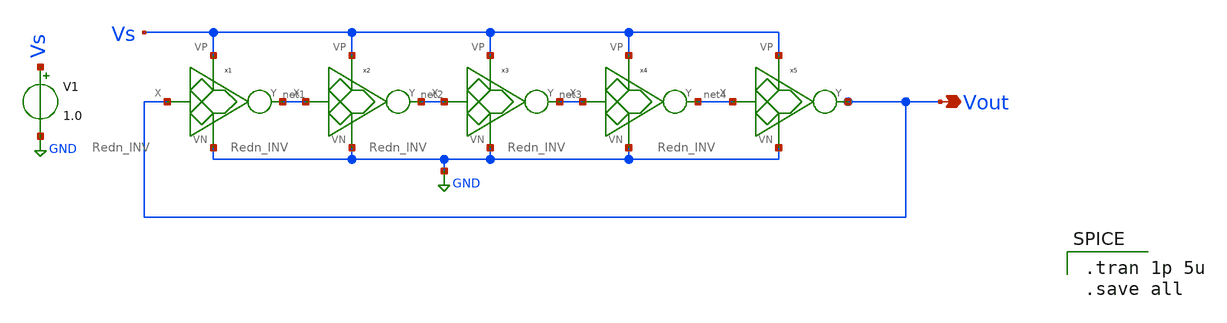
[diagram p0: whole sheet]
** sch_path: Blocks/Ring_Osci/Rdn_Rng_Osc.sch
**.subckt Rdn_Rng_Osc Vout
*.opin Vout
V1 Vs GND 1.0
x1 Vout net1 Vs GND Redn_INV
x2 net1 net2 Vs GND Redn_INV
x3 net2 net3 Vs GND Redn_INV
x4 net3 net4 Vs GND Redn_INV
x5 net4 Vout Vs GND Redn_INV
**** begin user architecture code

** opencircuitdesign pdks install
.lib $::SKYWATER_MODELS/sky130.lib.spice tt



.tran 1p 5u
.save all

**** end user architecture code
**.ends

* expanding   symbol:  Pico_project/Rdn_INV/Redn_INV.sym # of pins=4
** sym_path: component/Reduntant_Inverter/Redn_INV.sym
** sch_path: component/Reduntant_Inverter/Redn_INV.sch
.subckt Redn_INV X Y VP VN
*.opin Y
*.ipin X
*.iopin VP
*.iopin VN
XM15 net4 X VN VN sky130_fd_pr__nfet_01v8_lvt L=0.15 W=1 nf=1 ad='int((nf+1)/2) * W/nf * 0.29' as='int((nf+2)/2) * W/nf * 0.29'
+ pd='2*int((nf+1)/2) * (W/nf + 0.29)' ps='2*int((nf+2)/2) * (W/nf + 0.29)' nrd='0.29 / W' nrs='0.29 / W'
+ sa=0 sb=0 sd=0 mult=1 m=1
XM1 net5 X net3 VN sky130_fd_pr__nfet_01v8_lvt L=0.15 W=3.25 nf=1 ad='int((nf+1)/2) * W/nf * 0.29' as='int((nf+2)/2) * W/nf * 0.29'
+ pd='2*int((nf+1)/2) * (W/nf + 0.29)' ps='2*int((nf+2)/2) * (W/nf + 0.29)' nrd='0.29 / W' nrs='0.29 / W'
+ sa=0 sb=0 sd=0 mult=1 m=1
XM16 Y X net6 VN sky130_fd_pr__nfet_01v8_lvt L=0.15 W=6.5 nf=1 ad='int((nf+1)/2) * W/nf * 0.29' as='int((nf+2)/2) * W/nf * 0.29'
+ pd='2*int((nf+1)/2) * (W/nf + 0.29)' ps='2*int((nf+2)/2) * (W/nf + 0.29)' nrd='0.29 / W' nrs='0.29 / W'
+ sa=0 sb=0 sd=0 mult=1 m=1
XM17 net3 X VN VN sky130_fd_pr__nfet_01v8_lvt L=0.15 W=3.25 nf=1 ad='int((nf+1)/2) * W/nf * 0.29' as='int((nf+2)/2) * W/nf * 0.29'
+ pd='2*int((nf+1)/2) * (W/nf + 0.29)' ps='2*int((nf+2)/2) * (W/nf + 0.29)' nrd='0.29 / W' nrs='0.29 / W'
+ sa=0 sb=0 sd=0 mult=1 m=1
XM18 net2 X VN VN sky130_fd_pr__nfet_01v8_lvt L=0.15 W=1.5 nf=1 ad='int((nf+1)/2) * W/nf * 0.29' as='int((nf+2)/2) * W/nf * 0.29'
+ pd='2*int((nf+1)/2) * (W/nf + 0.29)' ps='2*int((nf+2)/2) * (W/nf + 0.29)' nrd='0.29 / W' nrs='0.29 / W'
+ sa=0 sb=0 sd=0 mult=1 m=1
XM19 net1 X VN VN sky130_fd_pr__nfet_01v8_lvt L=0.15 W=6.5 nf=1 ad='int((nf+1)/2) * W/nf * 0.29' as='int((nf+2)/2) * W/nf * 0.29'
+ pd='2*int((nf+1)/2) * (W/nf + 0.29)' ps='2*int((nf+2)/2) * (W/nf + 0.29)' nrd='0.29 / W' nrs='0.29 / W'
+ sa=0 sb=0 sd=0 mult=1 m=1
XM20 net6 X net1 VN sky130_fd_pr__nfet_01v8_lvt L=0.15 W=6.5 nf=1 ad='int((nf+1)/2) * W/nf * 0.29' as='int((nf+2)/2) * W/nf * 0.29'
+ pd='2*int((nf+1)/2) * (W/nf + 0.29)' ps='2*int((nf+2)/2) * (W/nf + 0.29)' nrd='0.29 / W' nrs='0.29 / W'
+ sa=0 sb=0 sd=0 mult=1 m=1
XM2 net4 X VP VP sky130_fd_pr__pfet_01v8 L=0.15 W=10 nf=1 ad='int((nf+1)/2) * W/nf * 0.29' as='int((nf+2)/2) * W/nf * 0.29'
+ pd='2*int((nf+1)/2) * (W/nf + 0.29)' ps='2*int((nf+2)/2) * (W/nf + 0.29)' nrd='0.29 / W' nrs='0.29 / W'
+ sa=0 sb=0 sd=0 mult=1 m=1
XM5 net5 X net4 net4 sky130_fd_pr__pfet_01v8 L=0.15 W=10 nf=1 ad='int((nf+1)/2) * W/nf * 0.29' as='int((nf+2)/2) * W/nf * 0.29'
+ pd='2*int((nf+1)/2) * (W/nf + 0.29)' ps='2*int((nf+2)/2) * (W/nf + 0.29)' nrd='0.29 / W' nrs='0.29 / W'
+ sa=0 sb=0 sd=0 mult=1 m=1
XM6 Y X net5 VP sky130_fd_pr__pfet_01v8 L=0.15 W=10 nf=1 ad='int((nf+1)/2) * W/nf * 0.29' as='int((nf+2)/2) * W/nf * 0.29'
+ pd='2*int((nf+1)/2) * (W/nf + 0.29)' ps='2*int((nf+2)/2) * (W/nf + 0.29)' nrd='0.29 / W' nrs='0.29 / W'
+ sa=0 sb=0 sd=0 mult=1 m=1
XM8 net3 X VP VP sky130_fd_pr__pfet_01v8 L=0.15 W=2 nf=1 ad='int((nf+1)/2) * W/nf * 0.29' as='int((nf+2)/2) * W/nf * 0.29'
+ pd='2*int((nf+1)/2) * (W/nf + 0.29)' ps='2*int((nf+2)/2) * (W/nf + 0.29)' nrd='0.29 / W' nrs='0.29 / W'
+ sa=0 sb=0 sd=0 mult=1 m=1
XM12 net2 X VP VP sky130_fd_pr__pfet_01v8 L=0.15 W=5 nf=1 ad='int((nf+1)/2) * W/nf * 0.29' as='int((nf+2)/2) * W/nf * 0.29'
+ pd='2*int((nf+1)/2) * (W/nf + 0.29)' ps='2*int((nf+2)/2) * (W/nf + 0.29)' nrd='0.29 / W' nrs='0.29 / W'
+ sa=0 sb=0 sd=0 mult=1 m=1
XM14 net6 X net2 VP sky130_fd_pr__pfet_01v8 L=0.15 W=5 nf=1 ad='int((nf+1)/2) * W/nf * 0.29' as='int((nf+2)/2) * W/nf * 0.29'
+ pd='2*int((nf+1)/2) * (W/nf + 0.29)' ps='2*int((nf+2)/2) * (W/nf + 0.29)' nrd='0.29 / W' nrs='0.29 / W'
+ sa=0 sb=0 sd=0 mult=1 m=1
XM21 net1 X VP VP sky130_fd_pr__pfet_01v8 L=0.15 W=1.5 nf=1 ad='int((nf+1)/2) * W/nf * 0.29' as='int((nf+2)/2) * W/nf * 0.29'
+ pd='2*int((nf+1)/2) * (W/nf + 0.29)' ps='2*int((nf+2)/2) * (W/nf + 0.29)' nrd='0.29 / W' nrs='0.29 / W'
+ sa=0 sb=0 sd=0 mult=1 m=1
.ends

.GLOBAL GND
.end
